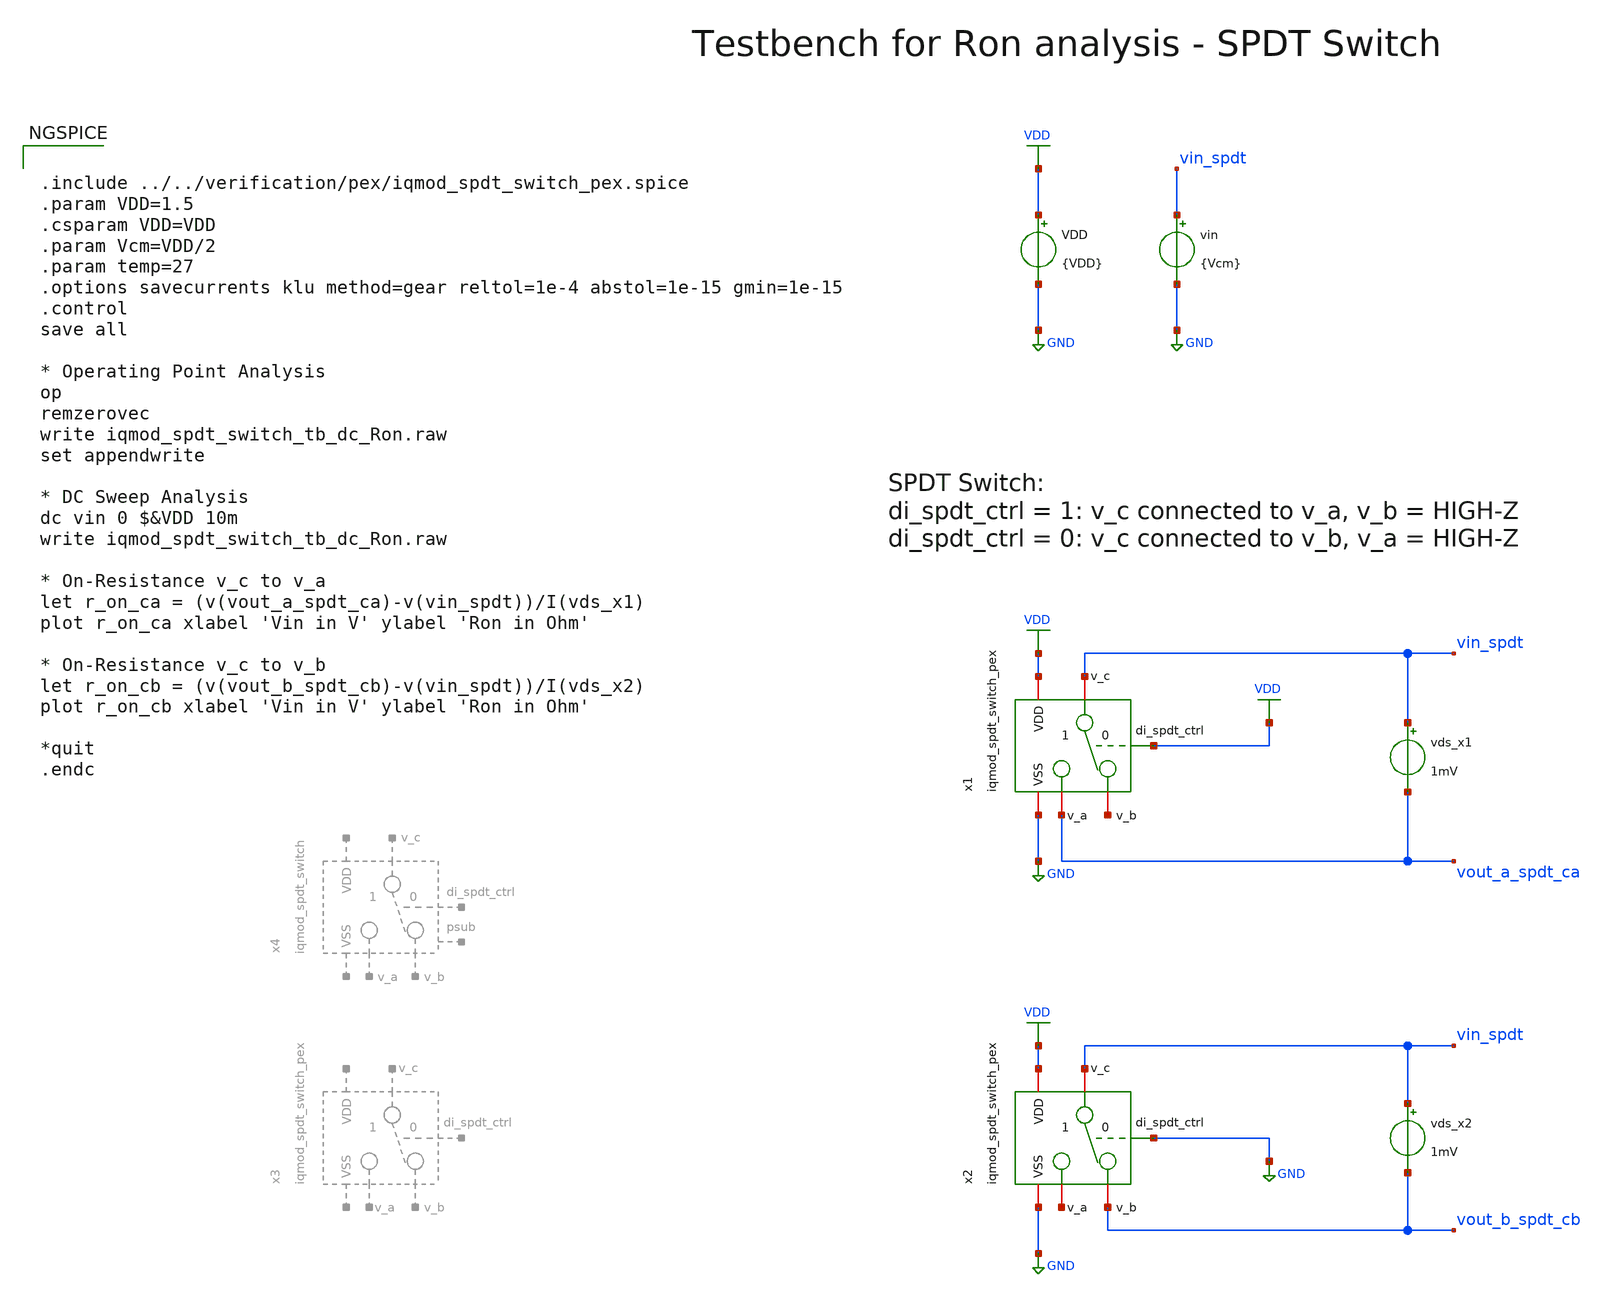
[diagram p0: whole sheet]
** sch_path: ihp130/macros/iqmod/xschem/testbenches/iqmod_spdt_switch_tb_dc_Ron.sch
**.subckt iqmod_spdt_switch_tb_dc_Ron
vds_x1 vin_spdt vout_a_spdt_ca 1mV
vds_x2 vin_spdt vout_b_spdt_cb 1mV
x1 VDD VDD GND vin_spdt net1 vout_a_spdt_ca iqmod_spdt_switch_pex
x2 VDD GND GND vin_spdt vout_b_spdt_cb net2 iqmod_spdt_switch_pex
vin vin_spdt GND {Vcm}
VDD VDD GND {VDD}
**** begin user architecture code


.include ../../verification/pex/iqmod_spdt_switch_pex.spice
.param VDD=1.5
.csparam VDD=VDD
.param Vcm=VDD/2
.param temp=27
.options savecurrents klu method=gear reltol=1e-4 abstol=1e-15 gmin=1e-15
.control
save all

* Operating Point Analysis
op
remzerovec
write iqmod_spdt_switch_tb_dc_Ron.raw
set appendwrite

* DC Sweep Analysis
dc vin 0 $&VDD 10m
write iqmod_spdt_switch_tb_dc_Ron.raw

* On-Resistance v_c to v_a
let r_on_ca = (v(vout_a_spdt_ca)-v(vin_spdt))/I(vds_x1)
plot r_on_ca xlabel 'Vin in V' ylabel 'Ron in Ohm'

* On-Resistance v_c to v_b
let r_on_cb = (v(vout_b_spdt_cb)-v(vin_spdt))/I(vds_x2)
plot r_on_cb xlabel 'Vin in V' ylabel 'Ron in Ohm'

*quit
.endc


.lib cornerMOSlv.lib mos_tt
.lib cornerMOShv.lib mos_tt
.lib cornerHBT.lib hbt_typ
.lib cornerRES.lib res_typ
.lib cornerCAP.lib cap_typ
.lib cornerDIO.lib dio_tt

**** end user architecture code
**.ends
.GLOBAL VDD
.GLOBAL GND
.end
